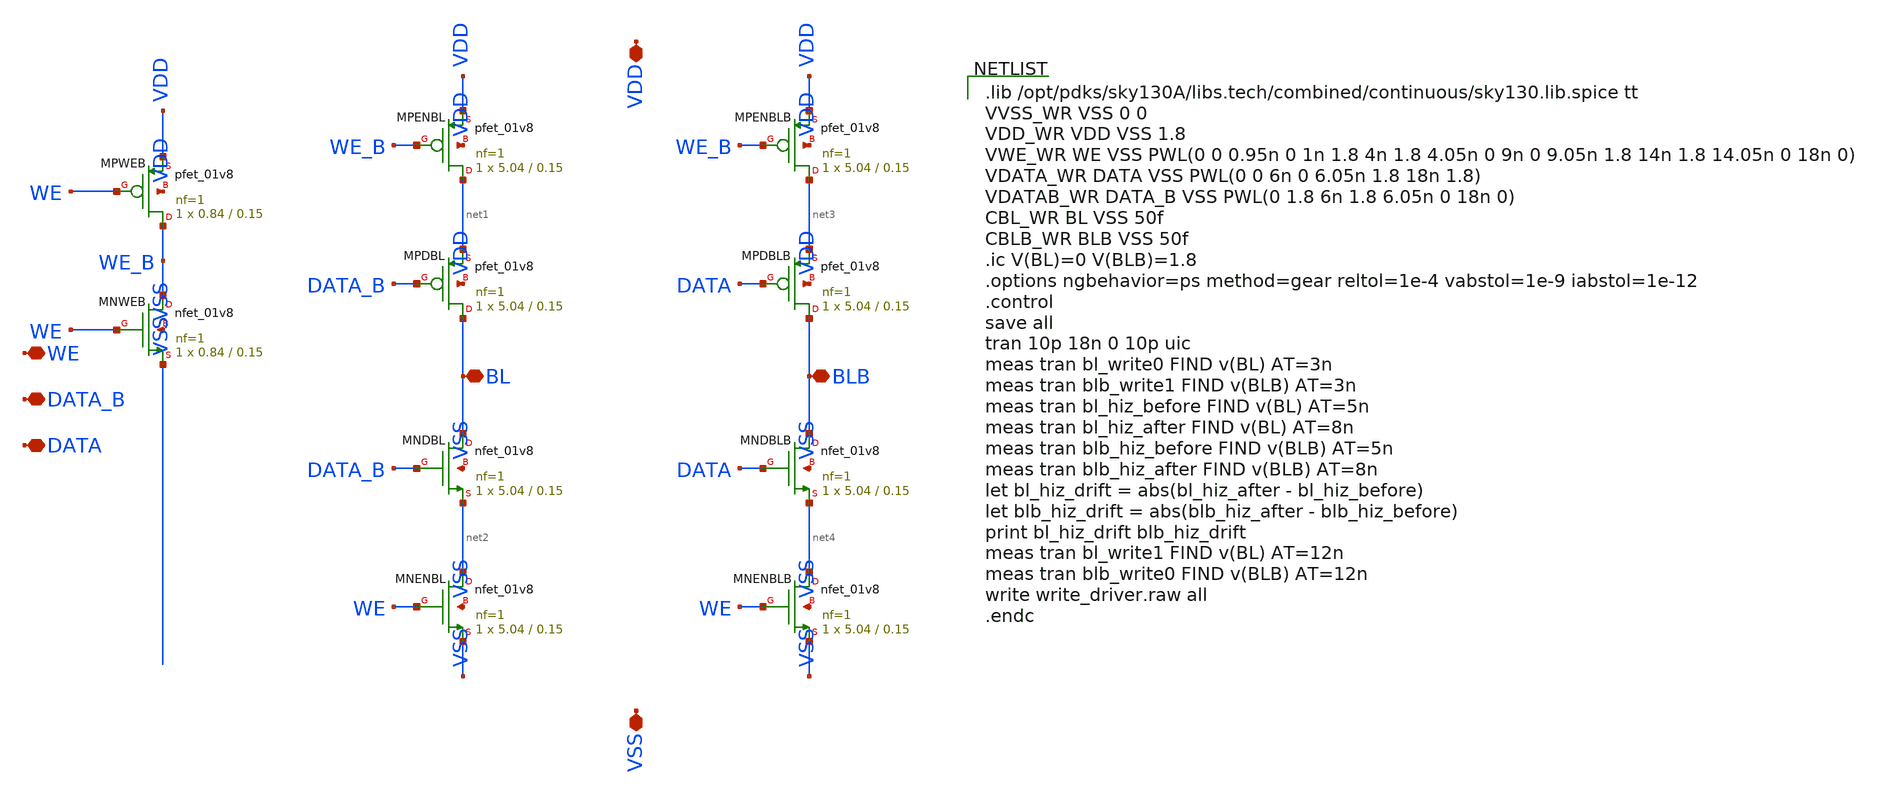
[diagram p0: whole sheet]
** sch_path: sims/integration/results/reconciliation_20261030/physical/cells/write_driver/write_driver.sch
**.subckt write_driver DATA DATA_B WE BL BLB VDD VSS
*.iopin DATA
*.iopin DATA_B
*.iopin WE
*.iopin BL
*.iopin BLB
*.iopin VDD
*.iopin VSS
XMPWEB WE_B WE VDD VDD sky130_fd_pr__pfet_01v8 L=0.15 W=0.84 nf=1 ad='int((nf+1)/2) * W/nf * 0.29' as='int((nf+2)/2) * W/nf * 0.29'
+ pd='2*int((nf+1)/2) * (W/nf + 0.29)' ps='2*int((nf+2)/2) * (W/nf + 0.29)' nrd='0.29 / W' nrs='0.29 / W'
+ sa=0 sb=0 sd=0 mult=1 m=1
XMNWEB WE_B WE VSS VSS sky130_fd_pr__nfet_01v8 L=0.15 W=0.84 nf=1 ad='int((1 + 1)/2) * 0.84 / 1 * 0.29'
+ as='int((1 + 2)/2) * 0.84 / 1 * 0.29' pd='2*int((1 + 1)/2) * (0.84 / 1 + 0.29)' ps='2*int((1 + 2)/2) * (0.84 / 1 + 0.29)'
+ nrd='0.29 / 0.84 ' nrs='0.29 / 0.84 ' sa=0 sb=0 sd=0 mult=1 m=1
XMPENBL net1 WE_B VDD VDD sky130_fd_pr__pfet_01v8 L=0.15 W=5.04 nf=1 ad='int((nf+1)/2) * W/nf * 0.29'
+ as='int((nf+2)/2) * W/nf * 0.29' pd='2*int((nf+1)/2) * (W/nf + 0.29)' ps='2*int((nf+2)/2) * (W/nf + 0.29)'
+ nrd='0.29 / W' nrs='0.29 / W' sa=0 sb=0 sd=0 mult=1 m=1
XMPDBL BL DATA_B net1 VDD sky130_fd_pr__pfet_01v8 L=0.15 W=5.04 nf=1 ad='int((nf+1)/2) * W/nf * 0.29'
+ as='int((nf+2)/2) * W/nf * 0.29' pd='2*int((nf+1)/2) * (W/nf + 0.29)' ps='2*int((nf+2)/2) * (W/nf + 0.29)'
+ nrd='0.29 / W' nrs='0.29 / W' sa=0 sb=0 sd=0 mult=1 m=1
XMNDBL BL DATA_B net2 VSS sky130_fd_pr__nfet_01v8 L=0.15 W=5.04 nf=1 ad='int((1 + 1)/2) * 5.04 / 1 * 0.29'
+ as='int((1 + 2)/2) * 5.04 / 1 * 0.29' pd='2*int((1 + 1)/2) * (5.04 / 1 + 0.29)' ps='2*int((1 + 2)/2) * (5.04 / 1 + 0.29)'
+ nrd='0.29 / 5.04 ' nrs='0.29 / 5.04 ' sa=0 sb=0 sd=0 mult=1 m=1
XMNENBL net2 WE VSS VSS sky130_fd_pr__nfet_01v8 L=0.15 W=5.04 nf=1 ad='int((1 + 1)/2) * 5.04 / 1 * 0.29'
+ as='int((1 + 2)/2) * 5.04 / 1 * 0.29' pd='2*int((1 + 1)/2) * (5.04 / 1 + 0.29)' ps='2*int((1 + 2)/2) * (5.04 / 1 + 0.29)'
+ nrd='0.29 / 5.04 ' nrs='0.29 / 5.04 ' sa=0 sb=0 sd=0 mult=1 m=1
XMPENBLB net3 WE_B VDD VDD sky130_fd_pr__pfet_01v8 L=0.15 W=5.04 nf=1 ad='int((nf+1)/2) * W/nf * 0.29'
+ as='int((nf+2)/2) * W/nf * 0.29' pd='2*int((nf+1)/2) * (W/nf + 0.29)' ps='2*int((nf+2)/2) * (W/nf + 0.29)'
+ nrd='0.29 / W' nrs='0.29 / W' sa=0 sb=0 sd=0 mult=1 m=1
XMPDBLB BLB DATA net3 VDD sky130_fd_pr__pfet_01v8 L=0.15 W=5.04 nf=1 ad='int((nf+1)/2) * W/nf * 0.29'
+ as='int((nf+2)/2) * W/nf * 0.29' pd='2*int((nf+1)/2) * (W/nf + 0.29)' ps='2*int((nf+2)/2) * (W/nf + 0.29)'
+ nrd='0.29 / W' nrs='0.29 / W' sa=0 sb=0 sd=0 mult=1 m=1
XMNDBLB BLB DATA net4 VSS sky130_fd_pr__nfet_01v8 L=0.15 W=5.04 nf=1 ad='int((1 + 1)/2) * 5.04 / 1 * 0.29'
+ as='int((1 + 2)/2) * 5.04 / 1 * 0.29' pd='2*int((1 + 1)/2) * (5.04 / 1 + 0.29)' ps='2*int((1 + 2)/2) * (5.04 / 1 + 0.29)'
+ nrd='0.29 / 5.04 ' nrs='0.29 / 5.04 ' sa=0 sb=0 sd=0 mult=1 m=1
XMNENBLB net4 WE VSS VSS sky130_fd_pr__nfet_01v8 L=0.15 W=5.04 nf=1 ad='int((1 + 1)/2) * 5.04 / 1 * 0.29'
+ as='int((1 + 2)/2) * 5.04 / 1 * 0.29' pd='2*int((1 + 1)/2) * (5.04 / 1 + 0.29)' ps='2*int((1 + 2)/2) * (5.04 / 1 + 0.29)'
+ nrd='0.29 / 5.04 ' nrs='0.29 / 5.04 ' sa=0 sb=0 sd=0 mult=1 m=1
**** begin user architecture code

.lib /opt/pdks/sky130A/libs.tech/combined/continuous/sky130.lib.spice tt
VVSS_WR VSS 0 0
VDD_WR VDD VSS 1.8
VWE_WR WE VSS PWL(0 0 0.95n 0 1n 1.8 4n 1.8 4.05n 0 9n 0 9.05n 1.8 14n 1.8 14.05n 0 18n 0)
VDATA_WR DATA VSS PWL(0 0 6n 0 6.05n 1.8 18n 1.8)
VDATAB_WR DATA_B VSS PWL(0 1.8 6n 1.8 6.05n 0 18n 0)
CBL_WR BL VSS 50f
CBLB_WR BLB VSS 50f
.ic V(BL)=0 V(BLB)=1.8
.options ngbehavior=ps method=gear reltol=1e-4 vabstol=1e-9 iabstol=1e-12
.control
save all
tran 10p 18n 0 10p uic
meas tran bl_write0 FIND v(BL) AT=3n
meas tran blb_write1 FIND v(BLB) AT=3n
meas tran bl_hiz_before FIND v(BL) AT=5n
meas tran bl_hiz_after FIND v(BL) AT=8n
meas tran blb_hiz_before FIND v(BLB) AT=5n
meas tran blb_hiz_after FIND v(BLB) AT=8n
let bl_hiz_drift = abs(bl_hiz_after - bl_hiz_before)
let blb_hiz_drift = abs(blb_hiz_after - blb_hiz_before)
print bl_hiz_drift blb_hiz_drift
meas tran bl_write1 FIND v(BL) AT=12n
meas tran blb_write0 FIND v(BLB) AT=12n
write write_driver.raw all
.endc

**** end user architecture code
**.ends
.end
